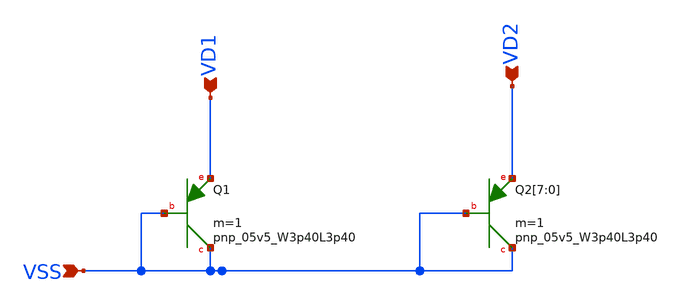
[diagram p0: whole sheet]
** sch_path: design/LELO_TEMP_SKY130A/LELOTEMP_BIPOLAR.sch
**.subckt LELOTEMP_BIPOLAR VSS VD1 VD2
*.ipin VSS
*.ipin VD1
*.ipin VD2
XQ1 VSS VSS VD1 sky130_fd_pr__pnp_05v5_W3p40L3p40 m=1
XQ2[7] VSS VSS VD2 sky130_fd_pr__pnp_05v5_W3p40L3p40 m=1
XQ2[6] VSS VSS VD2 sky130_fd_pr__pnp_05v5_W3p40L3p40 m=1
XQ2[5] VSS VSS VD2 sky130_fd_pr__pnp_05v5_W3p40L3p40 m=1
XQ2[4] VSS VSS VD2 sky130_fd_pr__pnp_05v5_W3p40L3p40 m=1
XQ2[3] VSS VSS VD2 sky130_fd_pr__pnp_05v5_W3p40L3p40 m=1
XQ2[2] VSS VSS VD2 sky130_fd_pr__pnp_05v5_W3p40L3p40 m=1
XQ2[1] VSS VSS VD2 sky130_fd_pr__pnp_05v5_W3p40L3p40 m=1
XQ2[0] VSS VSS VD2 sky130_fd_pr__pnp_05v5_W3p40L3p40 m=1
**.ends
.end
